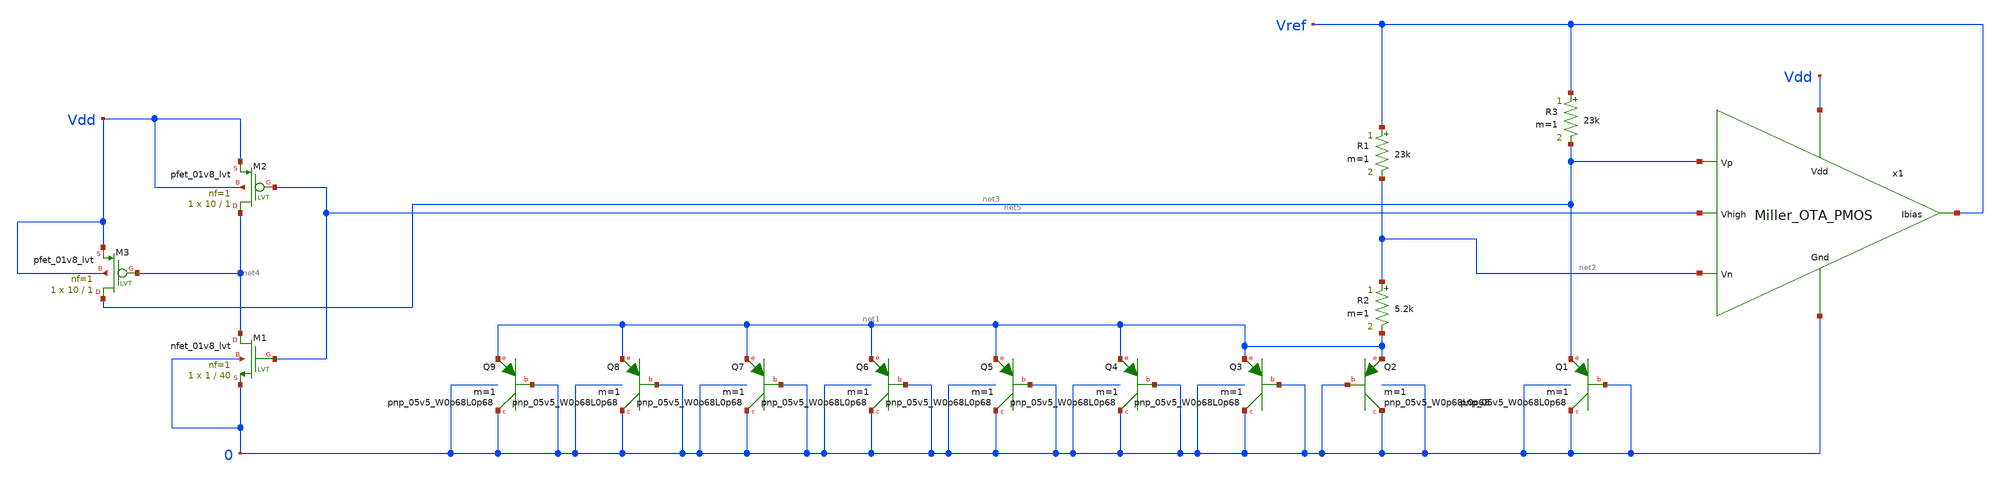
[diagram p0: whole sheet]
** sch_path: Bandgap/My Design/Schematics/Bandgap1.8v.sch
**.subckt Bandgap1.8v
R1 Vref net2 23k m=1
R2 net2 net1 5.2k m=1
R3 Vref net3 23k m=1
XQ1 0 0 net3 sky130_fd_pr__pnp_05v5_W0p68L0p68 m=1
XQ2 0 0 net1 sky130_fd_pr__pnp_05v5_W0p68L0p68 m=1
XQ3 0 0 net1 sky130_fd_pr__pnp_05v5_W0p68L0p68 m=1
XQ4 0 0 net1 sky130_fd_pr__pnp_05v5_W0p68L0p68 m=1
XQ5 0 0 net1 sky130_fd_pr__pnp_05v5_W0p68L0p68 m=1
XQ6 0 0 net1 sky130_fd_pr__pnp_05v5_W0p68L0p68 m=1
XQ7 0 0 net1 sky130_fd_pr__pnp_05v5_W0p68L0p68 m=1
XQ8 0 0 net1 sky130_fd_pr__pnp_05v5_W0p68L0p68 m=1
XQ9 0 0 net1 sky130_fd_pr__pnp_05v5_W0p68L0p68 m=1
x1 Vdd net3 net2 Vref net5 0 Miller_OTA_PMOS
XM1 net4 net5 0 0 sky130_fd_pr__nfet_01v8_lvt L=40 W=1 nf=1 ad='int((nf+1)/2) * W/nf * 0.29' as='int((nf+2)/2) * W/nf * 0.29'
+ pd='2*int((nf+1)/2) * (W/nf + 0.29)' ps='2*int((nf+2)/2) * (W/nf + 0.29)' nrd='0.29 / W' nrs='0.29 / W'
+ sa=0 sb=0 sd=0 mult=1 m=1
XM2 net4 net5 Vdd Vdd sky130_fd_pr__pfet_01v8_lvt L=1 W=10 nf=1 ad='int((nf+1)/2) * W/nf * 0.29' as='int((nf+2)/2) * W/nf * 0.29'
+ pd='2*int((nf+1)/2) * (W/nf + 0.29)' ps='2*int((nf+2)/2) * (W/nf + 0.29)' nrd='0.29 / W' nrs='0.29 / W'
+ sa=0 sb=0 sd=0 mult=1 m=1
XM3 net3 net4 Vdd Vdd sky130_fd_pr__pfet_01v8_lvt L=1 W=10 nf=1 ad='int((nf+1)/2) * W/nf * 0.29' as='int((nf+2)/2) * W/nf * 0.29'
+ pd='2*int((nf+1)/2) * (W/nf + 0.29)' ps='2*int((nf+2)/2) * (W/nf + 0.29)' nrd='0.29 / W' nrs='0.29 / W'
+ sa=0 sb=0 sd=0 mult=1 m=1
**** begin user architecture code


*DC analysis
*vin Vdd 0 1.8
*.op
*Temerature variation
*vin Vdd 0 1.8
*.DC TEMP -40 125 1
*Supply variation
*vin Vdd 0 1.8
*.DC vin 0 3 0.05
*Transient analysis
*vin Vdd 0 dc 0 pwl(0 0 100u 0 200u 3 500u 3)
*.tran 100u 500u
*PSRR analysis
*vin vdd 0 DC 1.8 AC 1
*.ac dec 10 1 100MEG
.end



.include $::SKYWATER_MODELS/cells/nfet_01v8/sky130_fd_pr__nfet_01v8__tt.corner.spice
.include $::SKYWATER_MODELS/cells/nfet_01v8_lvt/sky130_fd_pr__nfet_01v8_lvt__tt.corner.spice
.include $::SKYWATER_MODELS/cells/pfet_01v8/sky130_fd_pr__pfet_01v8__tt.corner.spice
.include $::SKYWATER_MODELS/cells/nfet_03v3_nvt/sky130_fd_pr__nfet_03v3_nvt__tt.corner.spice
.include $::SKYWATER_MODELS/cells/nfet_05v0_nvt/sky130_fd_pr__nfet_05v0_nvt__tt.corner.spice
.include $::SKYWATER_MODELS/cells/esd_nfet_01v8/sky130_fd_pr__esd_nfet_01v8__tt.corner.spice
.include $::SKYWATER_MODELS/cells/pfet_01v8_lvt/sky130_fd_pr__pfet_01v8_lvt__tt.corner.spice
.include $::SKYWATER_MODELS/cells/pfet_01v8_hvt/sky130_fd_pr__pfet_01v8_hvt__tt.corner.spice
.include $::SKYWATER_MODELS/cells/esd_pfet_g5v0d10v5/sky130_fd_pr__esd_pfet_g5v0d10v5__tt.corner.spice
.include $::SKYWATER_MODELS/cells/pfet_g5v0d10v5/sky130_fd_pr__pfet_g5v0d10v5__tt.corner.spice
.include $::SKYWATER_MODELS/cells/pfet_g5v0d16v0/sky130_fd_pr__pfet_g5v0d16v0__tt.corner.spice
.include $::SKYWATER_MODELS/cells/nfet_g5v0d10v5/sky130_fd_pr__nfet_g5v0d10v5__tt.corner.spice
.include $::SKYWATER_MODELS/cells/nfet_g5v0d16v0/sky130_fd_pr__nfet_g5v0d16v0__tt_discrete.corner.spice
.include $::SKYWATER_MODELS/cells/esd_nfet_g5v0d10v5/sky130_fd_pr__esd_nfet_g5v0d10v5__tt.corner.spice
.include $::SKYWATER_MODELS/models/corners/tt/nonfet.spice
* Mismatch parameters
.include $::SKYWATER_MODELS/cells/nfet_01v8/sky130_fd_pr__nfet_01v8__mismatch.corner.spice
.include $::SKYWATER_MODELS/cells/pfet_01v8/sky130_fd_pr__pfet_01v8__mismatch.corner.spice
.include $::SKYWATER_MODELS/cells/nfet_01v8_lvt/sky130_fd_pr__nfet_01v8_lvt__mismatch.corner.spice
.include $::SKYWATER_MODELS/cells/pfet_01v8_lvt/sky130_fd_pr__pfet_01v8_lvt__mismatch.corner.spice
.include $::SKYWATER_MODELS/cells/pfet_01v8_hvt/sky130_fd_pr__pfet_01v8_hvt__mismatch.corner.spice
.include $::SKYWATER_MODELS/cells/nfet_g5v0d10v5/sky130_fd_pr__nfet_g5v0d10v5__mismatch.corner.spice
.include $::SKYWATER_MODELS/cells/pfet_g5v0d10v5/sky130_fd_pr__pfet_g5v0d10v5__mismatch.corner.spice
.include $::SKYWATER_MODELS/cells/nfet_05v0_nvt/sky130_fd_pr__nfet_05v0_nvt__mismatch.corner.spice
.include $::SKYWATER_MODELS/cells/nfet_03v3_nvt/sky130_fd_pr__nfet_03v3_nvt__mismatch.corner.spice
* Resistor$::SKYWATER_MODELS/Capacitor
.include $::SKYWATER_MODELS/models/r+c/res_typical__cap_typical.spice
.include $::SKYWATER_MODELS/models/r+c/res_typical__cap_typical__lin.spice
* Special cells
.include $::SKYWATER_MODELS/models/corners/tt/specialized_cells.spice
* All models
.include $::SKYWATER_MODELS/models/all.spice
* Corner
.include $::SKYWATER_MODELS/models/corners/tt/rf.spice

**** end user architecture code
**.ends

* expanding   symbol:  /home/eslam/Analog_Design/OTA/Schematic/Miller_OTA_PMOS.sym # of pins=6
** sym_path: OTA/Schematic/Miller_OTA_PMOS.sym
** sch_path: OTA/Schematic/Miller_OTA_PMOS.sch
.subckt Miller_OTA_PMOS Vdd Vp Vn Ibias Vhigh Gnd
*.ipin Vp
*.ipin Vn
*.opin Ibias
*.ipin Vdd
*.ipin Gnd
*.ipin Vhigh
XM6 Ibias Vhigh Vdd Vdd sky130_fd_pr__pfet_g5v0d10v5 L=1 W=10 nf=1 ad='int((nf+1)/2) * W/nf * 0.29' as='int((nf+2)/2) * W/nf * 0.29'
+ pd='2*int((nf+1)/2) * (W/nf + 0.29)' ps='2*int((nf+2)/2) * (W/nf + 0.29)' nrd='0.29 / W' nrs='0.29 / W'
+ sa=0 sb=0 sd=0 mult=1 m=1
XM5 net3 Vhigh Vdd Vdd sky130_fd_pr__pfet_g5v0d10v5 L=1 W=10 nf=1 ad='int((nf+1)/2) * W/nf * 0.29' as='int((nf+2)/2) * W/nf * 0.29'
+ pd='2*int((nf+1)/2) * (W/nf + 0.29)' ps='2*int((nf+2)/2) * (W/nf + 0.29)' nrd='0.29 / W' nrs='0.29 / W'
+ sa=0 sb=0 sd=0 mult=1 m=1
XM7 Vhigh Vhigh Vdd Vdd sky130_fd_pr__pfet_g5v0d10v5 L=1 W=54 nf=1 ad='int((nf+1)/2) * W/nf * 0.29' as='int((nf+2)/2) * W/nf * 0.29'
+ pd='2*int((nf+1)/2) * (W/nf + 0.29)' ps='2*int((nf+2)/2) * (W/nf + 0.29)' nrd='0.29 / W' nrs='0.29 / W'
+ sa=0 sb=0 sd=0 mult=1 m=1
XC1 net1 Vhigh sky130_fd_pr__cap_mim_m3_2 W=1 L=1 MF=1 m=1
XM1 net2 Vn net3 Vdd sky130_fd_pr__pfet_g5v0d10v5 L=1 W=30 nf=1 ad='int((nf+1)/2) * W/nf * 0.29' as='int((nf+2)/2) * W/nf * 0.29'
+ pd='2*int((nf+1)/2) * (W/nf + 0.29)' ps='2*int((nf+2)/2) * (W/nf + 0.29)' nrd='0.29 / W' nrs='0.29 / W'
+ sa=0 sb=0 sd=0 mult=1 m=1
XM2 net1 Vp net3 Vdd sky130_fd_pr__pfet_g5v0d10v5 L=1 W=30 nf=1 ad='int((nf+1)/2) * W/nf * 0.29' as='int((nf+2)/2) * W/nf * 0.29'
+ pd='2*int((nf+1)/2) * (W/nf + 0.29)' ps='2*int((nf+2)/2) * (W/nf + 0.29)' nrd='0.29 / W' nrs='0.29 / W'
+ sa=0 sb=0 sd=0 mult=1 m=1
XM8 Vhigh net1 Gnd Gnd sky130_fd_pr__nfet_g5v0d10v5 L=0.5 W=75 nf=1 ad='int((nf+1)/2) * W/nf * 0.29'
+ as='int((nf+2)/2) * W/nf * 0.29' pd='2*int((nf+1)/2) * (W/nf + 0.29)' ps='2*int((nf+2)/2) * (W/nf + 0.29)'
+ nrd='0.29 / W' nrs='0.29 / W' sa=0 sb=0 sd=0 mult=1 m=1
XM4 net1 net2 Gnd Gnd sky130_fd_pr__nfet_g5v0d10v5 L=0.5 W=7.4 nf=1 ad='int((nf+1)/2) * W/nf * 0.29'
+ as='int((nf+2)/2) * W/nf * 0.29' pd='2*int((nf+1)/2) * (W/nf + 0.29)' ps='2*int((nf+2)/2) * (W/nf + 0.29)'
+ nrd='0.29 / W' nrs='0.29 / W' sa=0 sb=0 sd=0 mult=1 m=1
XM3 net2 net2 Gnd Gnd sky130_fd_pr__nfet_g5v0d10v5 L=0.5 W=7.4 nf=1 ad='int((nf+1)/2) * W/nf * 0.29'
+ as='int((nf+2)/2) * W/nf * 0.29' pd='2*int((nf+1)/2) * (W/nf + 0.29)' ps='2*int((nf+2)/2) * (W/nf + 0.29)'
+ nrd='0.29 / W' nrs='0.29 / W' sa=0 sb=0 sd=0 mult=1 m=1
.ends

.end
